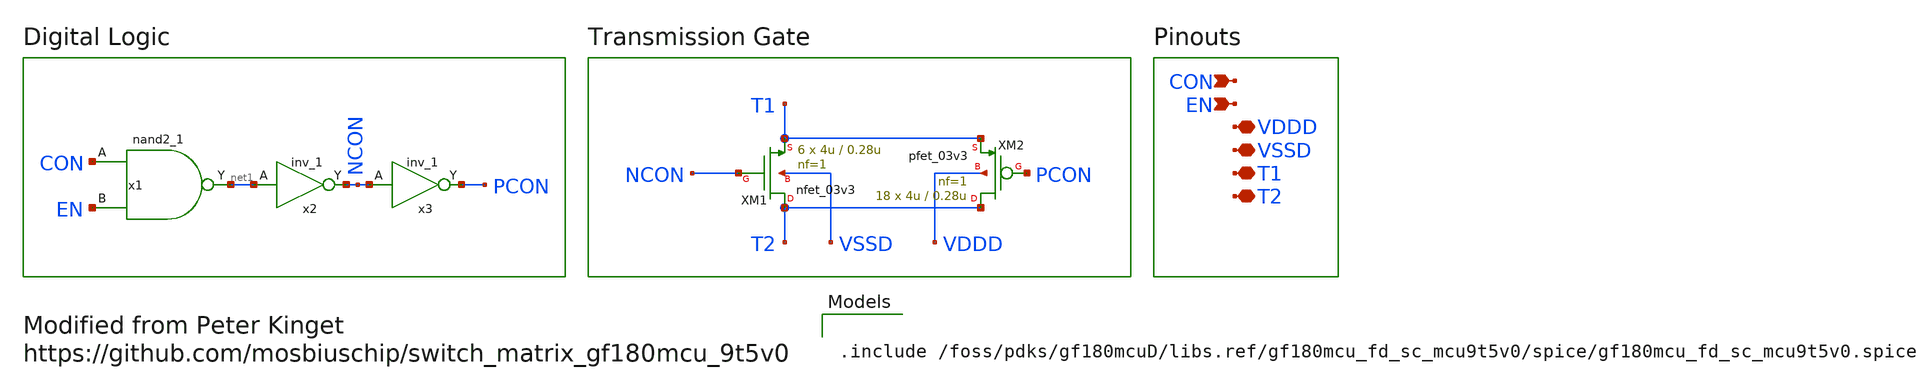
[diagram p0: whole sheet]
** sch_path: designs/libs/core_switch_matrix/tgate/tgate.sch
**.subckt tgate CON EN VDDD VSSD T1 T2
*.ipin CON
*.ipin EN
*.iopin VDDD
*.iopin VSSD
*.iopin T1
*.iopin T2
XM1 T2 NCON T1 VSSD nfet_03v3 L=0.28u W=4u nf=1 ad='int((nf+1)/2) * W/nf * 0.18u' as='int((nf+2)/2) * W/nf * 0.18u'
+ pd='2*int((nf+1)/2) * (W/nf + 0.18u)' ps='2*int((nf+2)/2) * (W/nf + 0.18u)' nrd='0.18u / W' nrs='0.18u / W'
+ sa=0 sb=0 sd=0 m=6
XM2 T2 PCON T1 VDDD pfet_03v3 L=0.28u W=4u nf=1 ad='int((nf+1)/2) * W/nf * 0.18u' as='int((nf+2)/2) * W/nf * 0.18u'
+ pd='2*int((nf+1)/2) * (W/nf + 0.18u)' ps='2*int((nf+2)/2) * (W/nf + 0.18u)' nrd='0.18u / W' nrs='0.18u / W'
+ sa=0 sb=0 sd=0 m=18
x1 CON EN VSSD VDDD VSSD VDDD net1 gf180mcu_fd_sc_mcu9t5v0__nand2_1
x2 net1 VSSD VDDD VSSD VDDD NCON gf180mcu_fd_sc_mcu9t5v0__inv_1
x3 NCON VSSD VDDD VSSD VDDD PCON gf180mcu_fd_sc_mcu9t5v0__inv_1
**** begin user architecture code

.include /foss/pdks/gf180mcuD/libs.ref/gf180mcu_fd_sc_mcu9t5v0/spice/gf180mcu_fd_sc_mcu9t5v0.spice

**** end user architecture code
**.ends
.end
